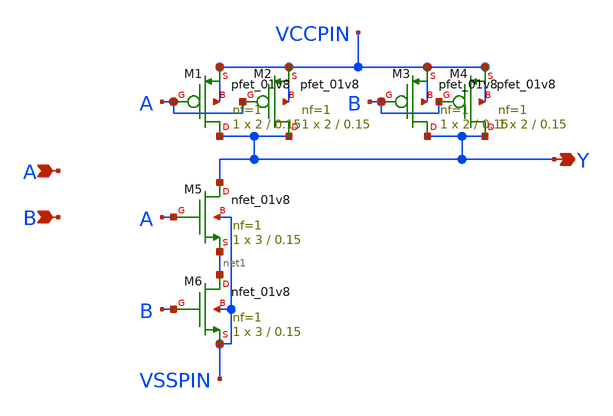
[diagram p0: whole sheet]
** sch_path: lib/xschem/NAND2X1.sch
**.subckt NAND2X1 A Y B
*.ipin A
*.opin Y
*.ipin B
XM1 Y A VCCPIN VCCPIN sky130_fd_pr__pfet_01v8 L=0.15 W=2 nf=1 ad='int((nf+1)/2) * W/nf * 0.29' as='int((nf+2)/2) * W/nf * 0.29'
+ pd='2*int((nf+1)/2) * (W/nf + 0.29)' ps='2*int((nf+2)/2) * (W/nf + 0.29)' nrd='0.29 / W' nrs='0.29 / W'
+ sa=0 sb=0 sd=0 mult=1 m=1
XM5 Y A net1 VSSPIN sky130_fd_pr__nfet_01v8 L=0.15 W=3 nf=1 ad='int((nf+1)/2) * W/nf * 0.29' as='int((nf+2)/2) * W/nf * 0.29'
+ pd='2*int((nf+1)/2) * (W/nf + 0.29)' ps='2*int((nf+2)/2) * (W/nf + 0.29)' nrd='0.29 / W' nrs='0.29 / W'
+ sa=0 sb=0 sd=0 mult=1 m=1
XM2 Y A VCCPIN VCCPIN sky130_fd_pr__pfet_01v8 L=0.15 W=2 nf=1 ad='int((nf+1)/2) * W/nf * 0.29' as='int((nf+2)/2) * W/nf * 0.29'
+ pd='2*int((nf+1)/2) * (W/nf + 0.29)' ps='2*int((nf+2)/2) * (W/nf + 0.29)' nrd='0.29 / W' nrs='0.29 / W'
+ sa=0 sb=0 sd=0 mult=1 m=1
XM3 Y B VCCPIN VCCPIN sky130_fd_pr__pfet_01v8 L=0.15 W=2 nf=1 ad='int((nf+1)/2) * W/nf * 0.29' as='int((nf+2)/2) * W/nf * 0.29'
+ pd='2*int((nf+1)/2) * (W/nf + 0.29)' ps='2*int((nf+2)/2) * (W/nf + 0.29)' nrd='0.29 / W' nrs='0.29 / W'
+ sa=0 sb=0 sd=0 mult=1 m=1
XM4 Y B VCCPIN VCCPIN sky130_fd_pr__pfet_01v8 L=0.15 W=2 nf=1 ad='int((nf+1)/2) * W/nf * 0.29' as='int((nf+2)/2) * W/nf * 0.29'
+ pd='2*int((nf+1)/2) * (W/nf + 0.29)' ps='2*int((nf+2)/2) * (W/nf + 0.29)' nrd='0.29 / W' nrs='0.29 / W'
+ sa=0 sb=0 sd=0 mult=1 m=1
XM6 net1 B VSSPIN VSSPIN sky130_fd_pr__nfet_01v8 L=0.15 W=3 nf=1 ad='int((nf+1)/2) * W/nf * 0.29' as='int((nf+2)/2) * W/nf * 0.29'
+ pd='2*int((nf+1)/2) * (W/nf + 0.29)' ps='2*int((nf+2)/2) * (W/nf + 0.29)' nrd='0.29 / W' nrs='0.29 / W'
+ sa=0 sb=0 sd=0 mult=1 m=1
**.ends
.end
